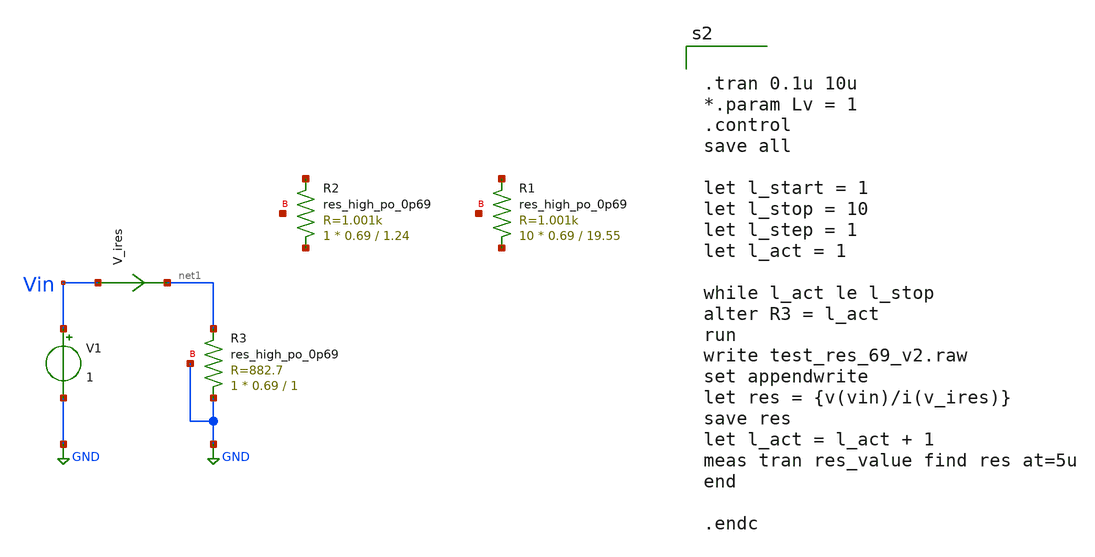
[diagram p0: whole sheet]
** sch_path: xschem/test_res_69_v2.sch
**.subckt test_res_69_v2
V1 Vin GND 1
V_ires Vin net1 0
.save i(v_ires)
XR1 net2 net3 net4 sky130_fd_pr__res_high_po_0p69 L=19.55 mult=10 m=10
XR2 net5 net6 net7 sky130_fd_pr__res_high_po_0p69 L=1.24 mult=1 m=1
XR3 GND net1 GND sky130_fd_pr__res_high_po_0p69 L=1 mult=1 m=1
**** begin user architecture code


.tran 0.1u 10u
*.param Lv = 1
.control
save all

let l_start = 1
let l_stop = 10
let l_step = 1
let l_act = 1

while l_act le l_stop
alter R3 = l_act
run
write test_res_69_v2.raw
set appendwrite
let res = {v(vin)/i(v_ires)}
save res
let l_act = l_act + 1
meas tran res_value find res at=5u
end

.endc


** opencircuitdesign pdks install
.lib $::SKYWATER_MODELS/sky130.lib.spice tt


**** end user architecture code
**.ends
.GLOBAL GND
.end
